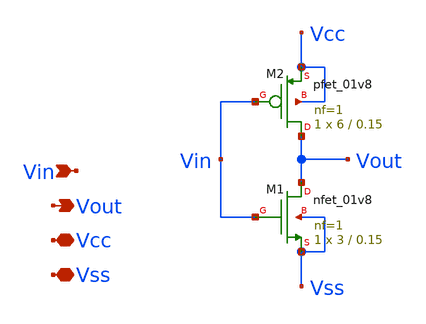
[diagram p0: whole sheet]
** sch_path: Git Files/Simulation Schematic/Pre Emphasis Driver/xor/inv111.sch
**.subckt inv111 Vin Vout Vcc Vss
*.ipin Vin
*.opin Vout
*.iopin Vcc
*.iopin Vss
XM2 Vout Vin Vcc Vcc sky130_fd_pr__pfet_01v8 L=0.15 W=6 nf=1 ad='int((nf+1)/2) * W/nf * 0.29' as='int((nf+2)/2) * W/nf * 0.29'
+ pd='2*int((nf+1)/2) * (W/nf + 0.29)' ps='2*int((nf+2)/2) * (W/nf + 0.29)' nrd='0.29 / W' nrs='0.29 / W'
+ sa=0 sb=0 sd=0 mult=1 m=1
XM1 Vout Vin Vss Vss sky130_fd_pr__nfet_01v8 L=0.15 W=3 nf=1 ad='int((nf+1)/2) * W/nf * 0.29' as='int((nf+2)/2) * W/nf * 0.29'
+ pd='2*int((nf+1)/2) * (W/nf + 0.29)' ps='2*int((nf+2)/2) * (W/nf + 0.29)' nrd='0.29 / W' nrs='0.29 / W'
+ sa=0 sb=0 sd=0 mult=1 m=1
**.ends
.end
